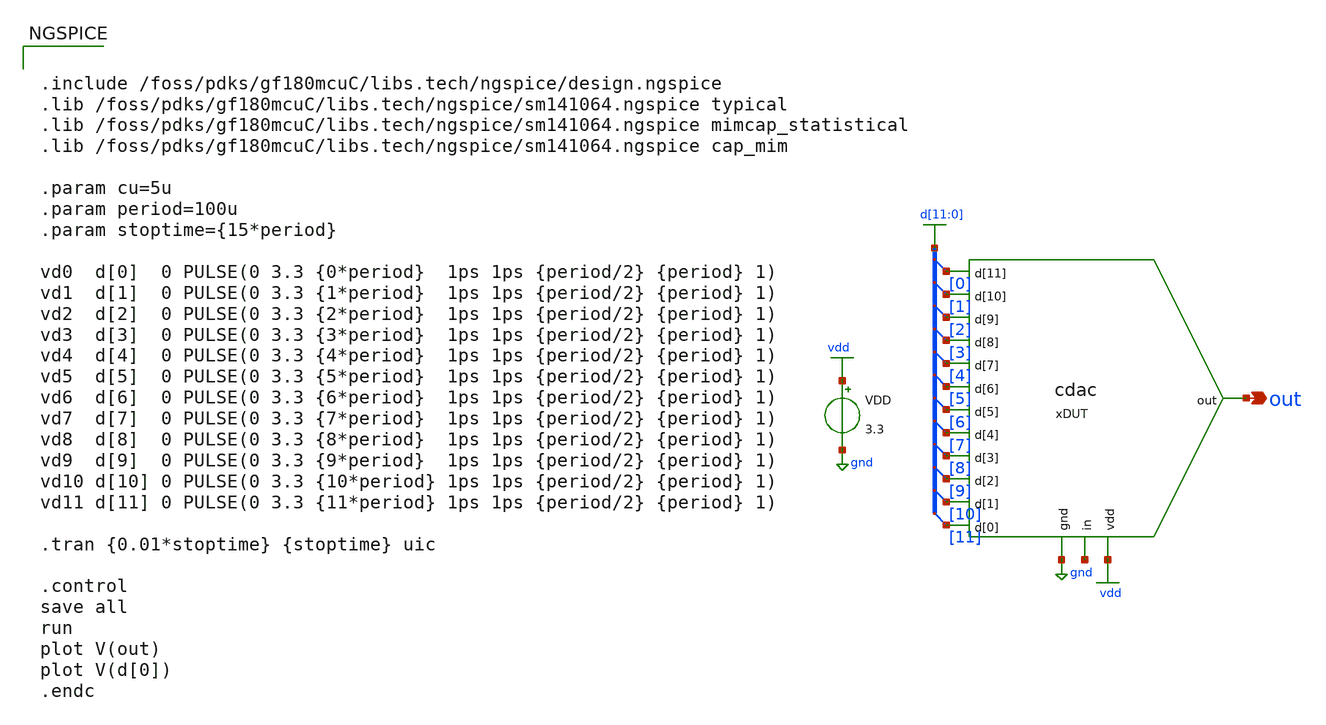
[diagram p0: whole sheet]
** sch_path: SAR_ADC/xschem/test/tb_cdac.sch
**.subckt tb_cdac out
*.opin out
* tap: d[11:0] --> d[11]
* tap: d[11:0] --> d[10]
* tap: d[11:0] --> d[9]
* tap: d[11:0] --> d[8]
* tap: d[11:0] --> d[7]
* tap: d[11:0] --> d[6]
* tap: d[11:0] --> d[5]
* tap: d[11:0] --> d[4]
* tap: d[11:0] --> d[3]
* tap: d[11:0] --> d[2]
* tap: d[11:0] --> d[1]
* tap: d[11:0] --> d[0]
VDD vdd gnd 3.3
xDUT out net1 d[2] d[4] d[11] d[0] d[8] d[7] d[9] d[10] d[3] d[5] d[6] d[1] gnd vdd cdac cu={cu}
**** begin user architecture code


.include /foss/pdks/gf180mcuC/libs.tech/ngspice/design.ngspice
.lib /foss/pdks/gf180mcuC/libs.tech/ngspice/sm141064.ngspice typical
.lib /foss/pdks/gf180mcuC/libs.tech/ngspice/sm141064.ngspice mimcap_statistical
.lib /foss/pdks/gf180mcuC/libs.tech/ngspice/sm141064.ngspice cap_mim

.param cu=5u
.param period=100u
.param stoptime={15*period}

vd0  d[0]  0 PULSE(0 3.3 {0*period}  1ps 1ps {period/2} {period} 1)
vd1  d[1]  0 PULSE(0 3.3 {1*period}  1ps 1ps {period/2} {period} 1)
vd2  d[2]  0 PULSE(0 3.3 {2*period}  1ps 1ps {period/2} {period} 1)
vd3  d[3]  0 PULSE(0 3.3 {3*period}  1ps 1ps {period/2} {period} 1)
vd4  d[4]  0 PULSE(0 3.3 {4*period}  1ps 1ps {period/2} {period} 1)
vd5  d[5]  0 PULSE(0 3.3 {5*period}  1ps 1ps {period/2} {period} 1)
vd6  d[6]  0 PULSE(0 3.3 {6*period}  1ps 1ps {period/2} {period} 1)
vd7  d[7]  0 PULSE(0 3.3 {7*period}  1ps 1ps {period/2} {period} 1)
vd8  d[8]  0 PULSE(0 3.3 {8*period}  1ps 1ps {period/2} {period} 1)
vd9  d[9]  0 PULSE(0 3.3 {9*period}  1ps 1ps {period/2} {period} 1)
vd10 d[10] 0 PULSE(0 3.3 {10*period} 1ps 1ps {period/2} {period} 1)
vd11 d[11] 0 PULSE(0 3.3 {11*period} 1ps 1ps {period/2} {period} 1)

.tran {0.01*stoptime} {stoptime} uic

.control
save all
run
plot V(out)
plot V(d[0])
.endc


**** end user architecture code
**.ends

* expanding   symbol:  ../spice/cdac.sym # of pins=16
** sym_path: SAR_ADC/xschem/spice/cdac.sym
** sch_path: SAR_ADC/xschem/spice/cdac.sch
.subckt cdac out in d[9] d[7] d[0] d[11] d[3] d[4] d[2] d[1] d[8] d[6] d[5] d[10] gnd vdd  cu=5u
*.ipin d[0]
*.ipin d[1]
*.ipin d[2]
*.ipin d[3]
*.ipin d[4]
*.ipin d[5]
*.ipin d[6]
*.ipin d[7]
*.ipin d[8]
*.ipin d[9]
*.ipin d[10]
*.ipin d[11]
*.ipin vdd
*.ipin gnd
*.opin out
*.iopin in
x1 in vdd gnd d[0] cdac_line CW={sqrt(2)*cu} CL={sqrt(2)*cu}
x2 in vdd gnd d[1] cdac_line CW={sqrt(3)*cu} CL={sqrt(3)*cu}
x3 in vdd gnd d[2] cdac_line CW={sqrt(4)*cu} CL={sqrt(4)*cu}
x4 in vdd gnd d[3] cdac_line CW={sqrt(8)*cu} CL={sqrt(8)*cu}
x5 in vdd gnd d[4] cdac_line CW={sqrt(16)*cu} CL={sqrt(16)*cu}
x6 in vdd gnd d[5] cdac_line CW={sqrt(32)*cu} CL={sqrt(32)*cu}
XCA out in cap_mim_1f5fF c_width={cu} c_length={cu} m=1
x7 out vdd gnd d[6] cdac_line CW={sqrt(1)*cu} CL={sqrt(1)*cu}
x8 out vdd gnd d[7] cdac_line CW={sqrt(2)*cu} CL={sqrt(2)*cu}
x9 out vdd gnd d[8] cdac_line CW={sqrt(4)*cu} CL={sqrt(4)*cu}
x10 out vdd gnd d[9] cdac_line CW={sqrt(8)*cu} CL={sqrt(8)*cu}
x11 out vdd gnd d[10] cdac_line CW={sqrt(16)*cu} CL={sqrt(16)*cu}
x12 out vdd gnd d[11] cdac_line CW={sqrt(32)*cu} CL={sqrt(32)*cu}
R1 out in 100T m=1
XC0 in gnd cap_mim_1f5fF c_width={cu} c_length={cu} m=1
.ends


* expanding   symbol:  /foss/designs/sar_adc/xschem/spice/cdac_line.sym # of pins=4
** sym_path: SAR_ADC/xschem/spice/cdac_line.sym
** sch_path: SAR_ADC/xschem/spice/cdac_line.sch
.subckt cdac_line vout vdd gnd vin  CW=1e-6 CL=1e-6
*.ipin vdd
*.ipin gnd
*.ipin vin
*.opin vout
x1 vdd gnd net1 net2 inv cl=0.28u wp=0.66u wn=0.22u
XC1 vout net1 cap_mim_2f0fF c_width=CW c_length=CL m=1
x2 vdd gnd net2 vin inv cl=0.28u wp=0.66u wn=0.22u
.ends


* expanding   symbol:  ../spice/inv.sym # of pins=4
** sym_path: SAR_ADC/xschem/spice/inv.sym
** sch_path: SAR_ADC/xschem/spice/inv.sch
.subckt inv vdd gnd vout vin  cl=0.28u wp=0.44u wn=0.22u
*.ipin gnd
*.ipin vdd
*.ipin vin
*.opin vout
XM1 gnd vin vout gnd nfet_03v3 L=0.28u W=4u nf=1 ad='int((nf+1)/2) * W/nf * 0.18u' as='int((nf+2)/2) * W/nf * 0.18u'
+ pd='2*int((nf+1)/2) * (W/nf + 0.18u)' ps='2*int((nf+2)/2) * (W/nf + 0.18u)' nrd='0.18u / W' nrs='0.18u / W'
+ sa=0 sb=0 sd=0 m=1
XM2 vdd vin vout vdd pfet_03v3 L=0.28u W=4u nf=1 ad='int((nf+1)/2) * W/nf * 0.18u' as='int((nf+2)/2) * W/nf * 0.18u'
+ pd='2*int((nf+1)/2) * (W/nf + 0.18u)' ps='2*int((nf+2)/2) * (W/nf + 0.18u)' nrd='0.18u / W' nrs='0.18u / W'
+ sa=0 sb=0 sd=0 m=1
.ends

.GLOBAL d[11:0]
.GLOBAL vdd
.GLOBAL gnd
.end
